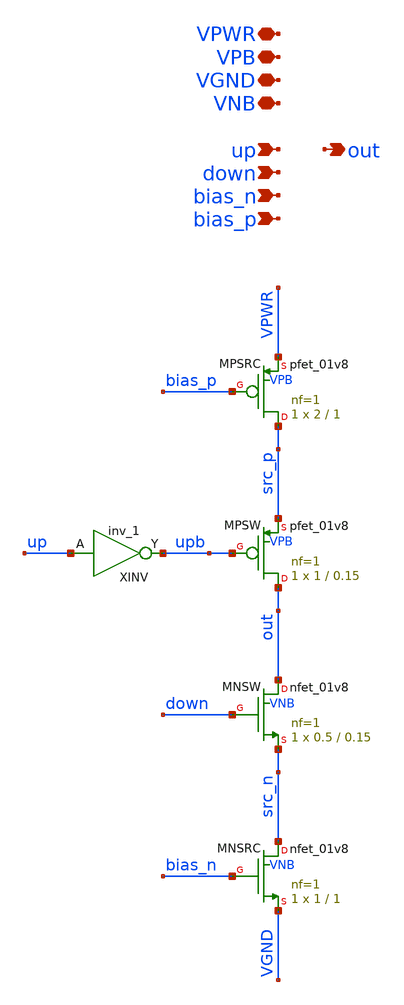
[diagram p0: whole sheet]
** sch_path: xschem/tiny_pll/tiny_pll_charge_pump.sch
**.subckt tiny_pll_charge_pump up down VNB VGND VPB VPWR out bias_n bias_p
*.ipin up
*.ipin down
*.iopin VNB
*.iopin VGND
*.iopin VPB
*.iopin VPWR
*.opin out
*.ipin bias_n
*.ipin bias_p
XMNSRC src_n bias_n VGND VNB sky130_fd_pr__nfet_01v8 L=1 W=1 nf=1 ad='int((nf+1)/2) * W/nf * 0.29' as='int((nf+2)/2) * W/nf * 0.29'
+ pd='2*int((nf+1)/2) * (W/nf + 0.29)' ps='2*int((nf+2)/2) * (W/nf + 0.29)' nrd='0.29 / W' nrs='0.29 / W'
+ sa=0 sb=0 sd=0 mult=1 m=1
XMNSW out down src_n VNB sky130_fd_pr__nfet_01v8 L=0.15 W=0.5 nf=1 ad='int((nf+1)/2) * W/nf * 0.29' as='int((nf+2)/2) * W/nf * 0.29'
+ pd='2*int((nf+1)/2) * (W/nf + 0.29)' ps='2*int((nf+2)/2) * (W/nf + 0.29)' nrd='0.29 / W' nrs='0.29 / W'
+ sa=0 sb=0 sd=0 mult=1 m=1
XMPSW out upb src_p VPB sky130_fd_pr__pfet_01v8 L=0.15 W=1 nf=1 ad='int((nf+1)/2) * W/nf * 0.29' as='int((nf+2)/2) * W/nf * 0.29'
+ pd='2*int((nf+1)/2) * (W/nf + 0.29)' ps='2*int((nf+2)/2) * (W/nf + 0.29)' nrd='0.29 / W' nrs='0.29 / W'
+ sa=0 sb=0 sd=0 mult=1 m=1
XMPSRC src_p bias_p VPWR VPB sky130_fd_pr__pfet_01v8 L=1 W=2 nf=1 ad='int((nf+1)/2) * W/nf * 0.29' as='int((nf+2)/2) * W/nf * 0.29'
+ pd='2*int((nf+1)/2) * (W/nf + 0.29)' ps='2*int((nf+2)/2) * (W/nf + 0.29)' nrd='0.29 / W' nrs='0.29 / W'
+ sa=0 sb=0 sd=0 mult=1 m=1
XINV up VGND VNB VPB VPWR upb sky130_fd_sc_hd__inv_1
**.ends
.end
